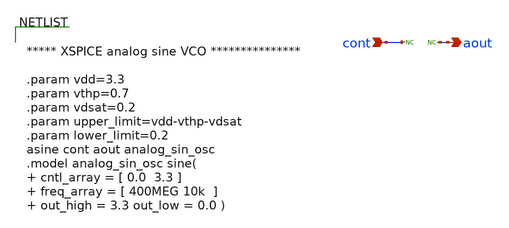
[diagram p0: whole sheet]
** sch_path: designs/libs/model_pll/vco_model.sch
**.subckt vco_model cont aout
*.ipin cont
*.opin aout
* noconn aout
* noconn cont
**** begin user architecture code


***** XSPICE analog sine VCO ***************

.param vdd=3.3
.param vthp=0.7
.param vdsat=0.2
.param upper_limit=vdd-vthp-vdsat
.param lower_limit=0.2
asine cont aout analog_sin_osc
.model analog_sin_osc sine(  cntl_array = [ 0.0  3.3 ]   freq_array = [ 400MEG 10k  ]  out_high =
+ 3.3 out_low = 0.0 )


**** end user architecture code
**.ends
.end
